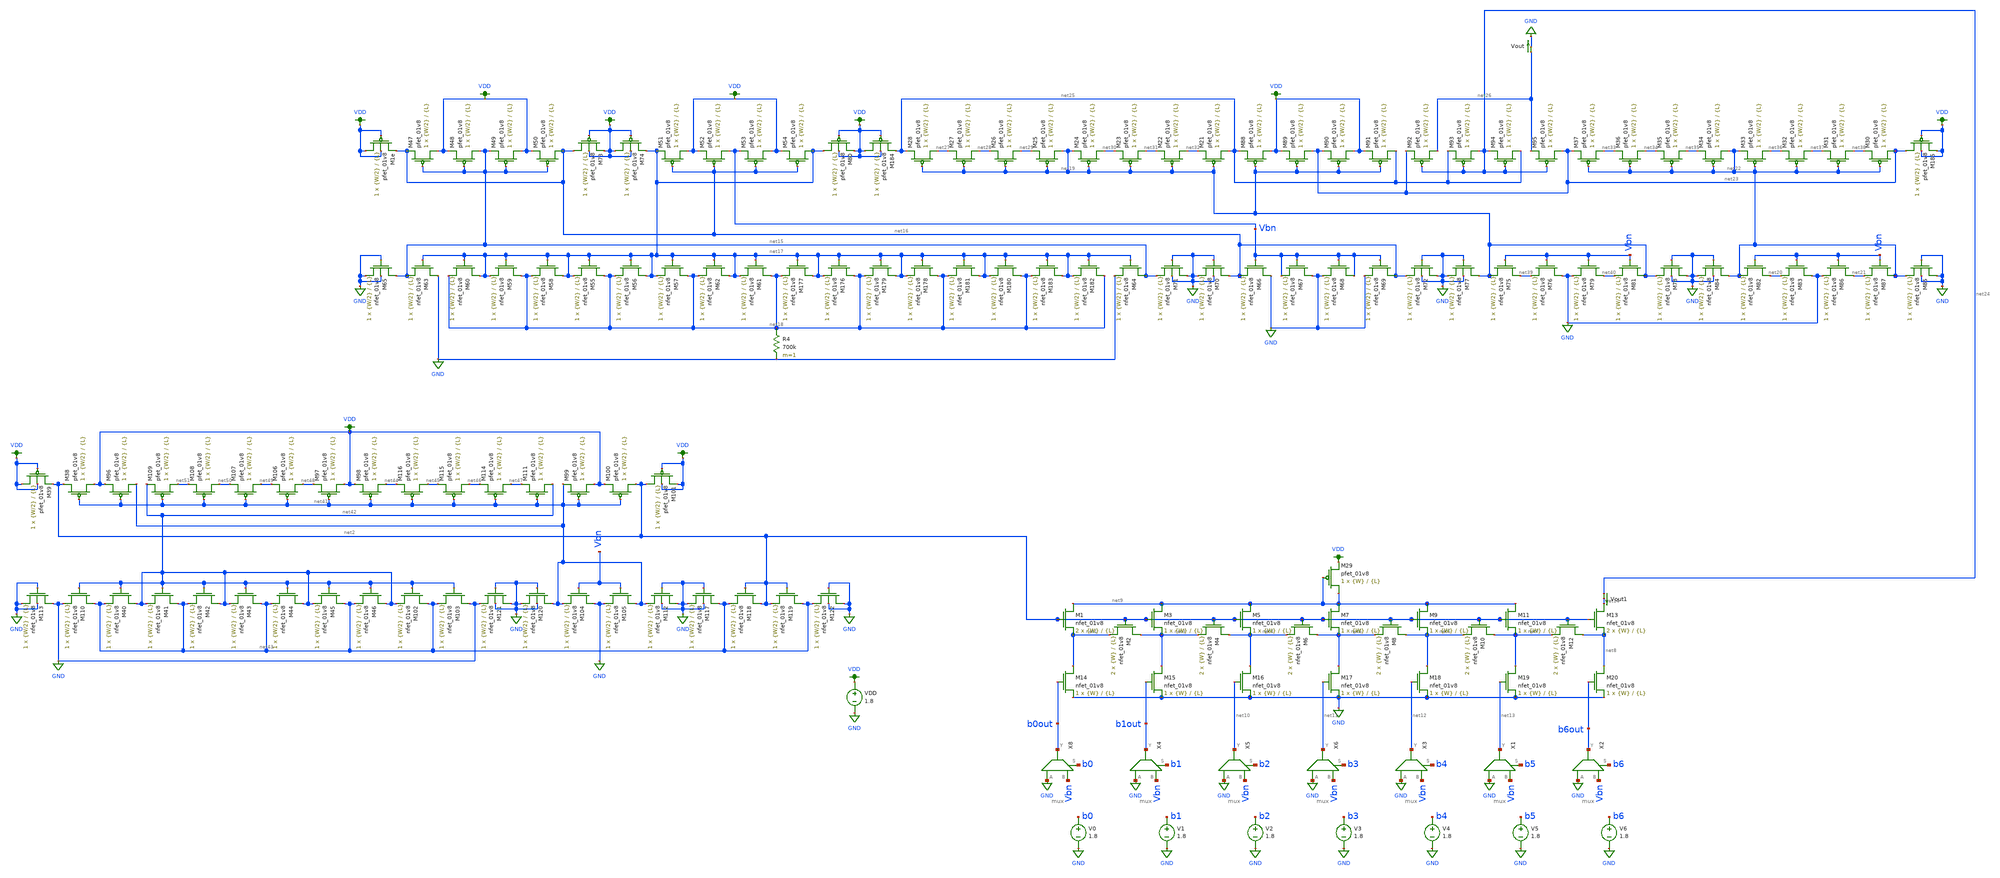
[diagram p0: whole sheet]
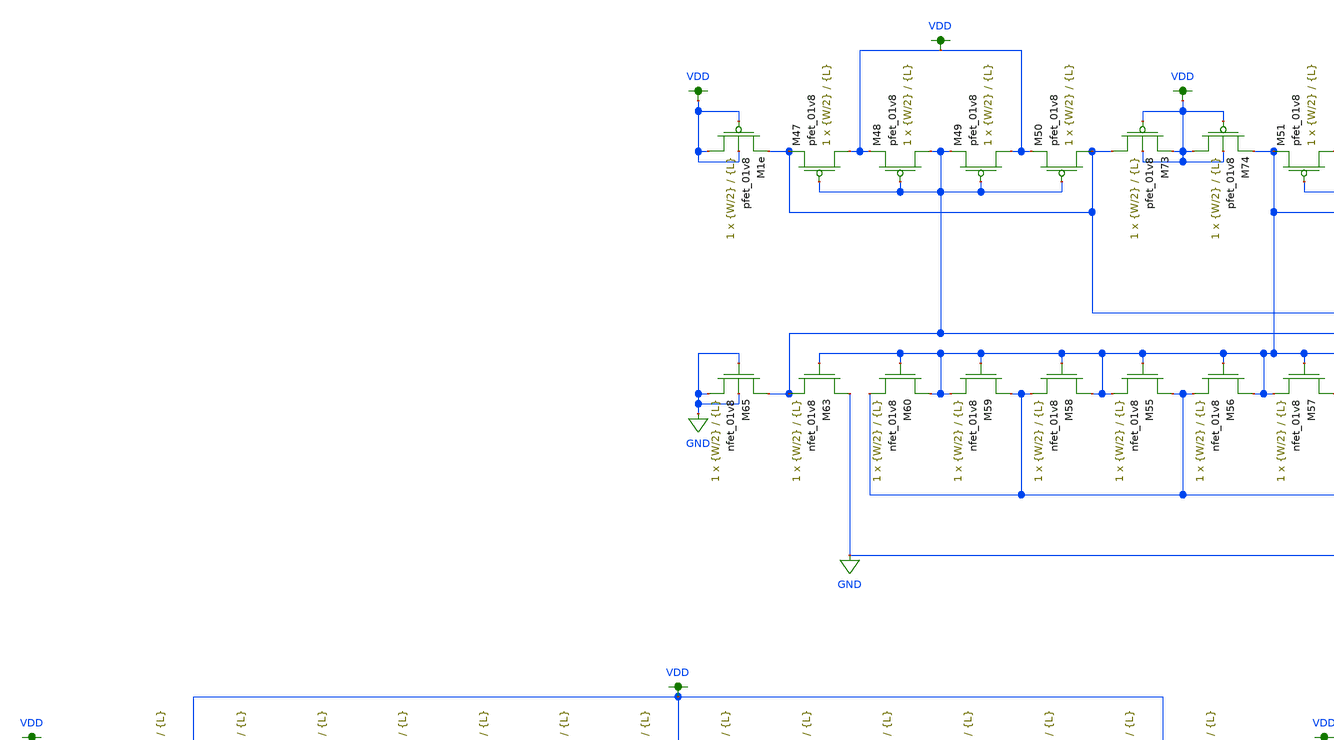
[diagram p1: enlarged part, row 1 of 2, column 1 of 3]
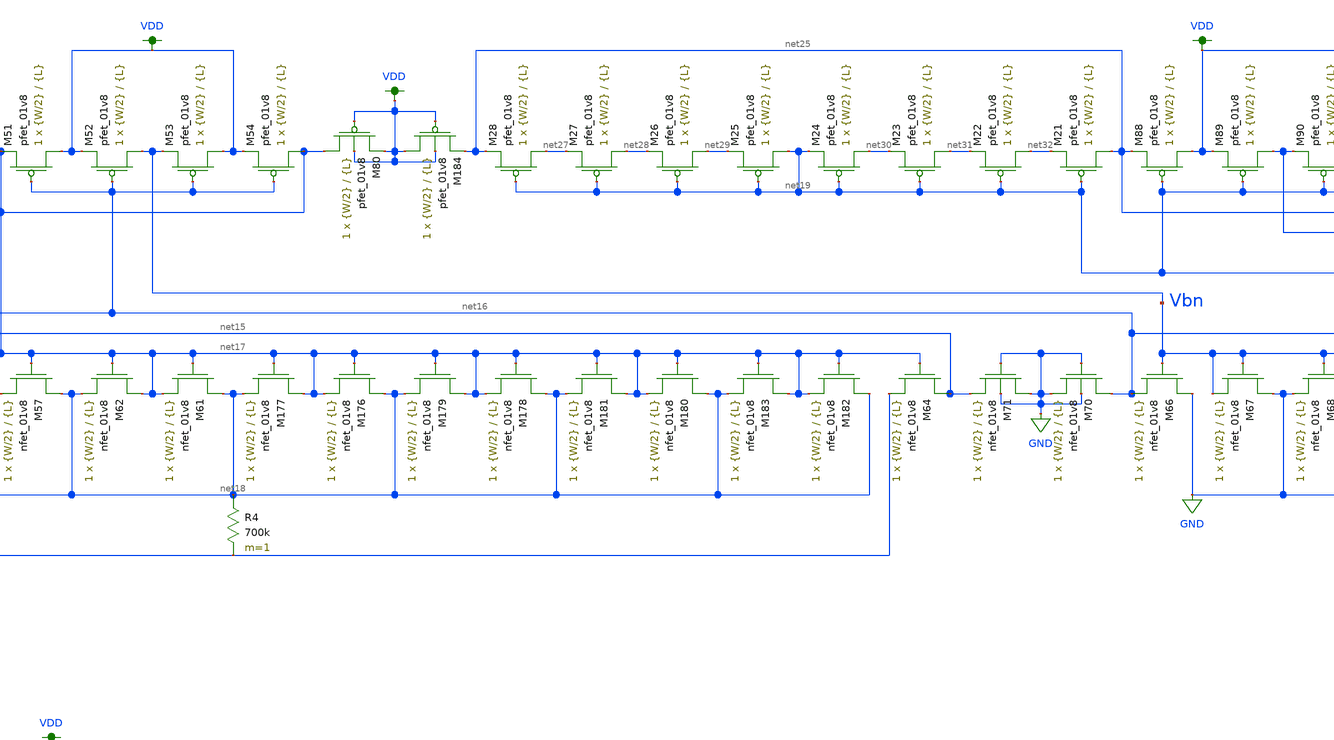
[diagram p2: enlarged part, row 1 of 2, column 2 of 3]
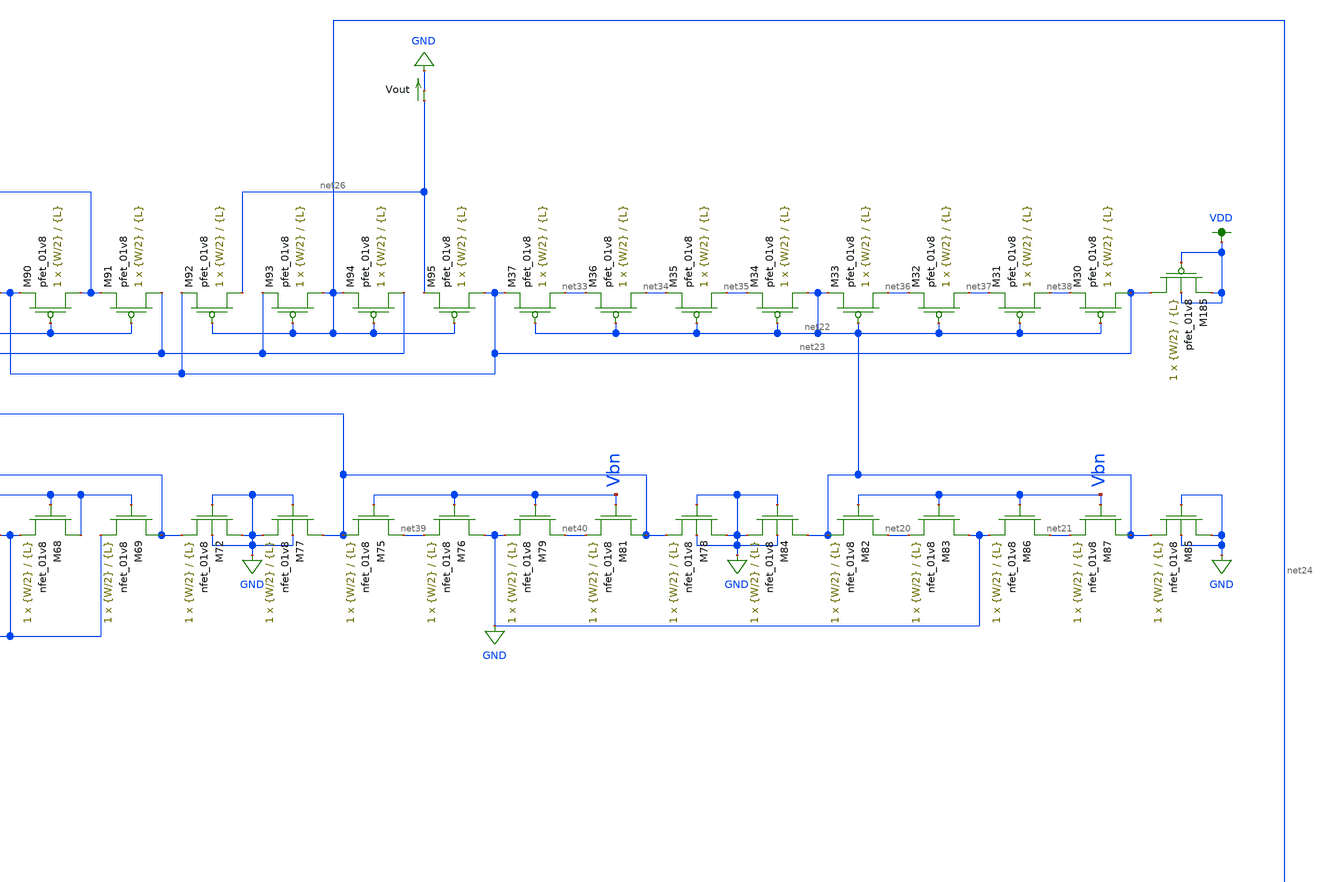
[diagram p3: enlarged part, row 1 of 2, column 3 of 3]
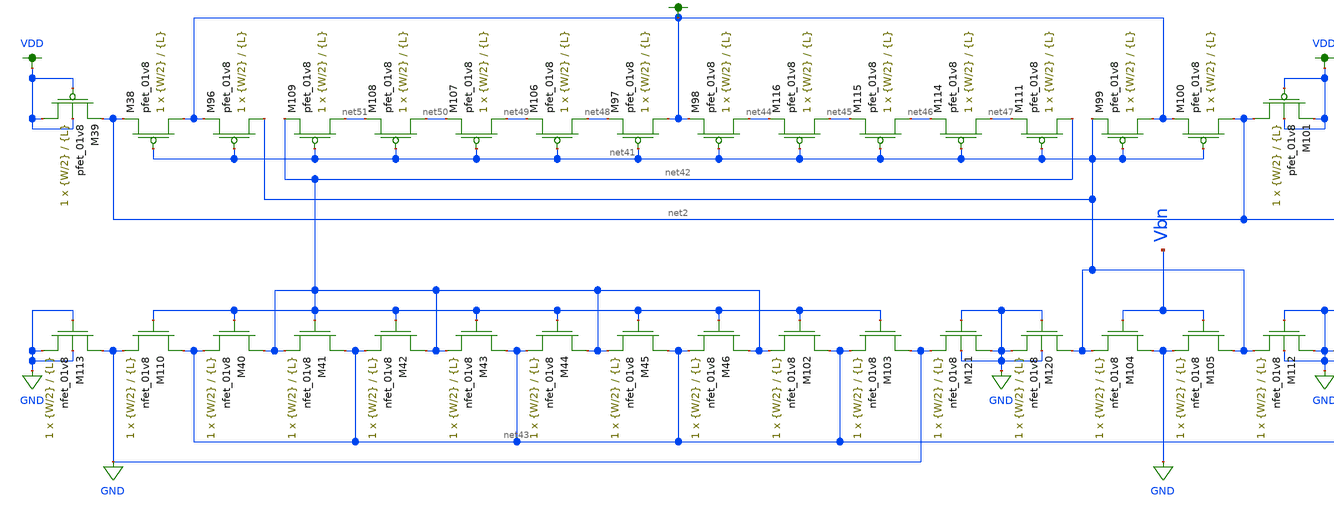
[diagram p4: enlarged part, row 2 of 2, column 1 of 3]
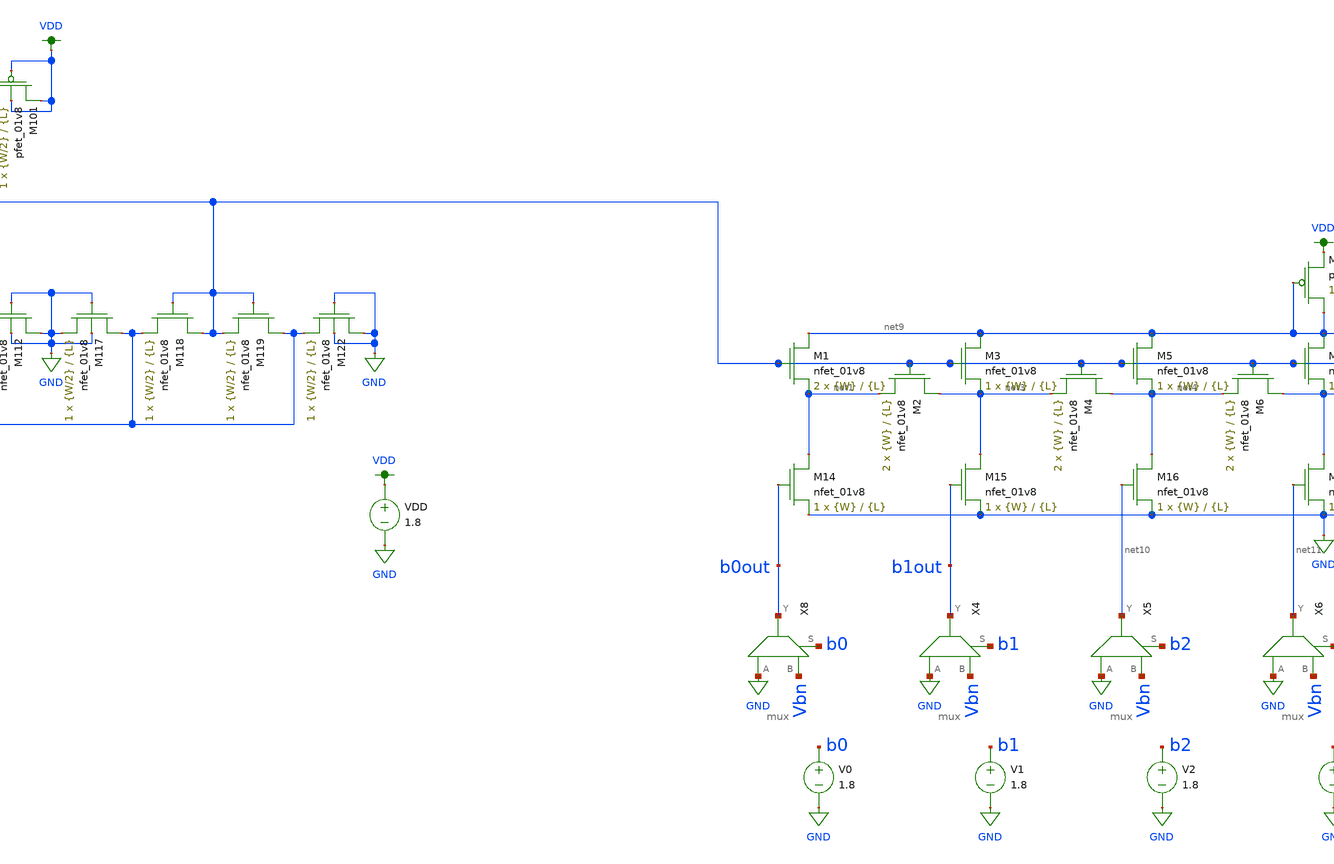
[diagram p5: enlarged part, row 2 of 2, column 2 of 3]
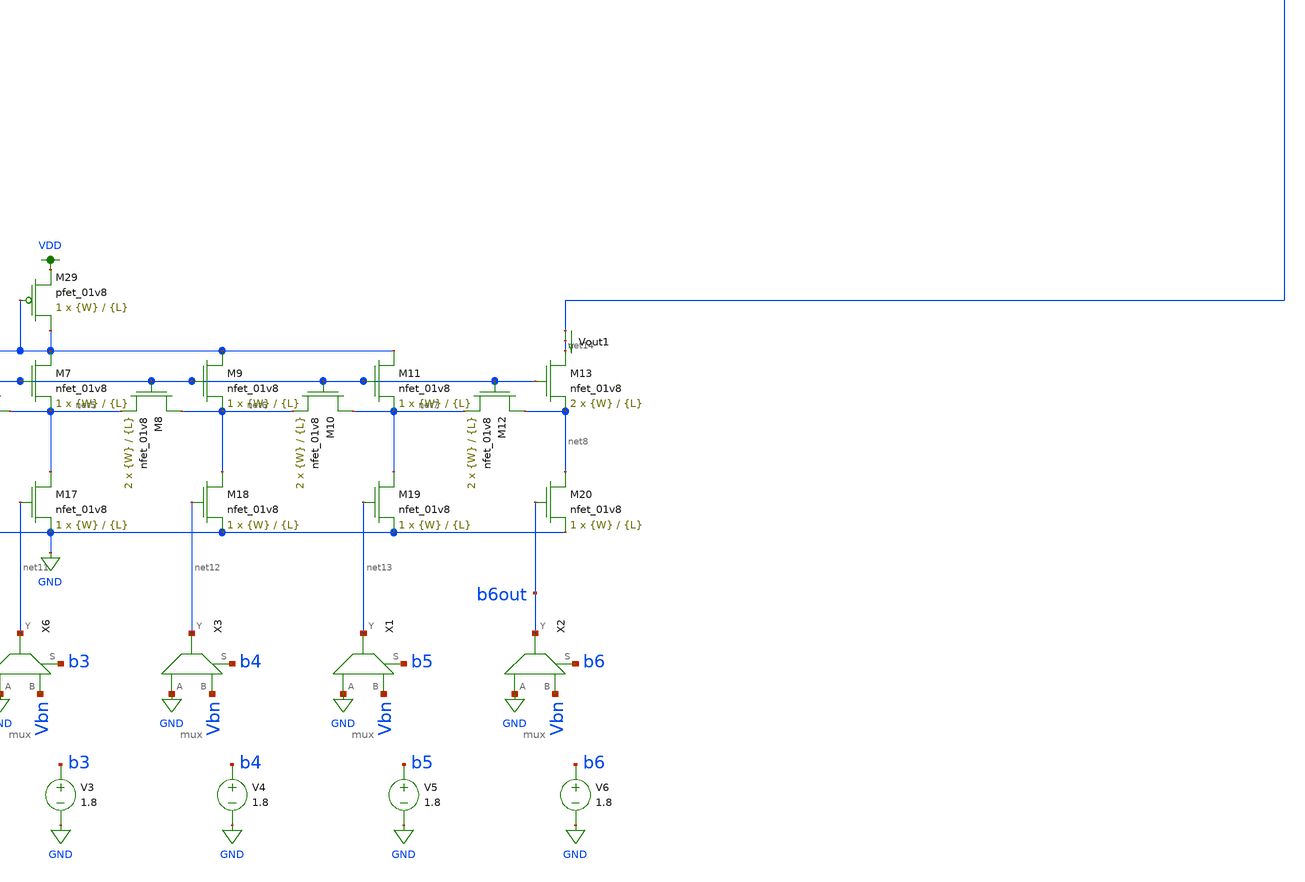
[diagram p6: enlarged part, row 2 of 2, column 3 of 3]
** sch_path: schematics/dac_dnl_inl_current_mirror_lds.sch
**.subckt dac_dnl_inl_current_mirror_lds
XM1 net9 net2 net1 GND sky130_fd_pr__nfet_01v8 L={L} W={W} nf=1 ad='int((nf+1)/2) * W/nf * 0.29' as='int((nf+2)/2) * W/nf * 0.29'
+ pd='2*int((nf+1)/2) * (W/nf + 0.29)' ps='2*int((nf+2)/2) * (W/nf + 0.29)' nrd='0.29 / W' nrs='0.29 / W'
+ sa=0 sb=0 sd=0 mult=2 m=2
XM2 net3 net2 net1 GND sky130_fd_pr__nfet_01v8 L={L} W={W} nf=1 ad='int((nf+1)/2) * W/nf * 0.29' as='int((nf+2)/2) * W/nf * 0.29'
+ pd='2*int((nf+1)/2) * (W/nf + 0.29)' ps='2*int((nf+2)/2) * (W/nf + 0.29)' nrd='0.29 / W' nrs='0.29 / W'
+ sa=0 sb=0 sd=0 mult=2 m=2
XM3 net9 net2 net3 GND sky130_fd_pr__nfet_01v8 L={L} W={W} nf=1 ad='int((nf+1)/2) * W/nf * 0.29' as='int((nf+2)/2) * W/nf * 0.29'
+ pd='2*int((nf+1)/2) * (W/nf + 0.29)' ps='2*int((nf+2)/2) * (W/nf + 0.29)' nrd='0.29 / W' nrs='0.29 / W'
+ sa=0 sb=0 sd=0 mult=1 m=1
XM4 net4 net2 net3 GND sky130_fd_pr__nfet_01v8 L={L} W={W} nf=1 ad='int((nf+1)/2) * W/nf * 0.29' as='int((nf+2)/2) * W/nf * 0.29'
+ pd='2*int((nf+1)/2) * (W/nf + 0.29)' ps='2*int((nf+2)/2) * (W/nf + 0.29)' nrd='0.29 / W' nrs='0.29 / W'
+ sa=0 sb=0 sd=0 mult=2 m=2
XM5 net9 net2 net4 GND sky130_fd_pr__nfet_01v8 L={L} W={W} nf=1 ad='int((nf+1)/2) * W/nf * 0.29' as='int((nf+2)/2) * W/nf * 0.29'
+ pd='2*int((nf+1)/2) * (W/nf + 0.29)' ps='2*int((nf+2)/2) * (W/nf + 0.29)' nrd='0.29 / W' nrs='0.29 / W'
+ sa=0 sb=0 sd=0 mult=1 m=1
XM6 net5 net2 net4 GND sky130_fd_pr__nfet_01v8 L={L} W={W} nf=1 ad='int((nf+1)/2) * W/nf * 0.29' as='int((nf+2)/2) * W/nf * 0.29'
+ pd='2*int((nf+1)/2) * (W/nf + 0.29)' ps='2*int((nf+2)/2) * (W/nf + 0.29)' nrd='0.29 / W' nrs='0.29 / W'
+ sa=0 sb=0 sd=0 mult=2 m=2
XM7 net9 net2 net5 GND sky130_fd_pr__nfet_01v8 L={L} W={W} nf=1 ad='int((nf+1)/2) * W/nf * 0.29' as='int((nf+2)/2) * W/nf * 0.29'
+ pd='2*int((nf+1)/2) * (W/nf + 0.29)' ps='2*int((nf+2)/2) * (W/nf + 0.29)' nrd='0.29 / W' nrs='0.29 / W'
+ sa=0 sb=0 sd=0 mult=1 m=1
XM8 net6 net2 net5 GND sky130_fd_pr__nfet_01v8 L={L} W={W} nf=1 ad='int((nf+1)/2) * W/nf * 0.29' as='int((nf+2)/2) * W/nf * 0.29'
+ pd='2*int((nf+1)/2) * (W/nf + 0.29)' ps='2*int((nf+2)/2) * (W/nf + 0.29)' nrd='0.29 / W' nrs='0.29 / W'
+ sa=0 sb=0 sd=0 mult=2 m=2
XM9 net9 net2 net6 GND sky130_fd_pr__nfet_01v8 L={L} W={W} nf=1 ad='int((nf+1)/2) * W/nf * 0.29' as='int((nf+2)/2) * W/nf * 0.29'
+ pd='2*int((nf+1)/2) * (W/nf + 0.29)' ps='2*int((nf+2)/2) * (W/nf + 0.29)' nrd='0.29 / W' nrs='0.29 / W'
+ sa=0 sb=0 sd=0 mult=1 m=1
XM10 net7 net2 net6 GND sky130_fd_pr__nfet_01v8 L={L} W={W} nf=1 ad='int((nf+1)/2) * W/nf * 0.29' as='int((nf+2)/2) * W/nf * 0.29'
+ pd='2*int((nf+1)/2) * (W/nf + 0.29)' ps='2*int((nf+2)/2) * (W/nf + 0.29)' nrd='0.29 / W' nrs='0.29 / W'
+ sa=0 sb=0 sd=0 mult=2 m=2
XM11 net9 net2 net7 GND sky130_fd_pr__nfet_01v8 L={L} W={W} nf=1 ad='int((nf+1)/2) * W/nf * 0.29' as='int((nf+2)/2) * W/nf * 0.29'
+ pd='2*int((nf+1)/2) * (W/nf + 0.29)' ps='2*int((nf+2)/2) * (W/nf + 0.29)' nrd='0.29 / W' nrs='0.29 / W'
+ sa=0 sb=0 sd=0 mult=1 m=1
XM12 net8 net2 net7 GND sky130_fd_pr__nfet_01v8 L={L} W={W} nf=1 ad='int((nf+1)/2) * W/nf * 0.29' as='int((nf+2)/2) * W/nf * 0.29'
+ pd='2*int((nf+1)/2) * (W/nf + 0.29)' ps='2*int((nf+2)/2) * (W/nf + 0.29)' nrd='0.29 / W' nrs='0.29 / W'
+ sa=0 sb=0 sd=0 mult=2 m=2
XM13 net14 net2 net8 GND sky130_fd_pr__nfet_01v8 L={L} W={W} nf=1 ad='int((nf+1)/2) * W/nf * 0.29' as='int((nf+2)/2) * W/nf * 0.29'
+ pd='2*int((nf+1)/2) * (W/nf + 0.29)' ps='2*int((nf+2)/2) * (W/nf + 0.29)' nrd='0.29 / W' nrs='0.29 / W'
+ sa=0 sb=0 sd=0 mult=2 m=2
XM14 net1 b0out GND GND sky130_fd_pr__nfet_01v8 L={L} W={W} nf=1 ad='int((nf+1)/2) * W/nf * 0.29' as='int((nf+2)/2) * W/nf * 0.29'
+ pd='2*int((nf+1)/2) * (W/nf + 0.29)' ps='2*int((nf+2)/2) * (W/nf + 0.29)' nrd='0.29 / W' nrs='0.29 / W'
+ sa=0 sb=0 sd=0 mult=1 m=1
XM15 net3 b1out GND GND sky130_fd_pr__nfet_01v8 L={L} W={W} nf=1 ad='int((nf+1)/2) * W/nf * 0.29' as='int((nf+2)/2) * W/nf * 0.29'
+ pd='2*int((nf+1)/2) * (W/nf + 0.29)' ps='2*int((nf+2)/2) * (W/nf + 0.29)' nrd='0.29 / W' nrs='0.29 / W'
+ sa=0 sb=0 sd=0 mult=1 m=1
XM16 net4 net10 GND GND sky130_fd_pr__nfet_01v8 L={L} W={W} nf=1 ad='int((nf+1)/2) * W/nf * 0.29' as='int((nf+2)/2) * W/nf * 0.29'
+ pd='2*int((nf+1)/2) * (W/nf + 0.29)' ps='2*int((nf+2)/2) * (W/nf + 0.29)' nrd='0.29 / W' nrs='0.29 / W'
+ sa=0 sb=0 sd=0 mult=1 m=1
XM17 net5 net11 GND GND sky130_fd_pr__nfet_01v8 L={L} W={W} nf=1 ad='int((nf+1)/2) * W/nf * 0.29' as='int((nf+2)/2) * W/nf * 0.29'
+ pd='2*int((nf+1)/2) * (W/nf + 0.29)' ps='2*int((nf+2)/2) * (W/nf + 0.29)' nrd='0.29 / W' nrs='0.29 / W'
+ sa=0 sb=0 sd=0 mult=1 m=1
XM18 net6 net12 GND GND sky130_fd_pr__nfet_01v8 L={L} W={W} nf=1 ad='int((nf+1)/2) * W/nf * 0.29' as='int((nf+2)/2) * W/nf * 0.29'
+ pd='2*int((nf+1)/2) * (W/nf + 0.29)' ps='2*int((nf+2)/2) * (W/nf + 0.29)' nrd='0.29 / W' nrs='0.29 / W'
+ sa=0 sb=0 sd=0 mult=1 m=1
XM19 net7 net13 GND GND sky130_fd_pr__nfet_01v8 L={L} W={W} nf=1 ad='int((nf+1)/2) * W/nf * 0.29' as='int((nf+2)/2) * W/nf * 0.29'
+ pd='2*int((nf+1)/2) * (W/nf + 0.29)' ps='2*int((nf+2)/2) * (W/nf + 0.29)' nrd='0.29 / W' nrs='0.29 / W'
+ sa=0 sb=0 sd=0 mult=1 m=1
XM20 net8 b6out GND GND sky130_fd_pr__nfet_01v8 L={L} W={W} nf=1 ad='int((nf+1)/2) * W/nf * 0.29' as='int((nf+2)/2) * W/nf * 0.29'
+ pd='2*int((nf+1)/2) * (W/nf + 0.29)' ps='2*int((nf+2)/2) * (W/nf + 0.29)' nrd='0.29 / W' nrs='0.29 / W'
+ sa=0 sb=0 sd=0 mult=1 m=1
V0 b0 GND 1.8
V1 b1 GND 1.8
V2 b2 GND 1.8
V3 b3 GND 1.8
V4 b4 GND 1.8
V5 b5 GND 1.8
V6 b6 GND 1.8
VDD VDD GND 1.8
XM29 net9 net9 VDD VDD sky130_fd_pr__pfet_01v8 L={L} W={W} nf=1 ad='int((nf+1)/2) * W/nf * 0.29' as='int((nf+2)/2) * W/nf * 0.29'
+ pd='2*int((nf+1)/2) * (W/nf + 0.29)' ps='2*int((nf+2)/2) * (W/nf + 0.29)' nrd='0.29 / W' nrs='0.29 / W'
+ sa=0 sb=0 sd=0 mult=1 m=1
X8 GND Vbn b0out b0 mux
X4 GND Vbn b1out b1 mux
X5 GND Vbn net10 b2 mux
X6 GND Vbn net11 b3 mux
X3 GND Vbn net12 b4 mux
X1 GND Vbn net13 b5 mux
X2 GND Vbn b6out b6 mux
Vout1 net24 net14 0
.save i(vout1)
XM47 VDD net15 net16 VDD sky130_fd_pr__pfet_01v8 L={L} W={W/2} nf=1 ad='int((nf+1)/2) * W/nf * 0.29'
+ as='int((nf+2)/2) * W/nf * 0.29' pd='2*int((nf+1)/2) * (W/nf + 0.29)' ps='2*int((nf+2)/2) * (W/nf + 0.29)'
+ nrd='0.29 / W' nrs='0.29 / W' sa=0 sb=0 sd=0 mult=1 m=1
XM48 net15 net15 VDD VDD sky130_fd_pr__pfet_01v8 L={L} W={W/2} nf=1 ad='int((nf+1)/2) * W/nf * 0.29'
+ as='int((nf+2)/2) * W/nf * 0.29' pd='2*int((nf+1)/2) * (W/nf + 0.29)' ps='2*int((nf+2)/2) * (W/nf + 0.29)'
+ nrd='0.29 / W' nrs='0.29 / W' sa=0 sb=0 sd=0 mult=1 m=1
XM49 VDD net15 net15 VDD sky130_fd_pr__pfet_01v8 L={L} W={W/2} nf=1 ad='int((nf+1)/2) * W/nf * 0.29'
+ as='int((nf+2)/2) * W/nf * 0.29' pd='2*int((nf+1)/2) * (W/nf + 0.29)' ps='2*int((nf+2)/2) * (W/nf + 0.29)'
+ nrd='0.29 / W' nrs='0.29 / W' sa=0 sb=0 sd=0 mult=1 m=1
XM50 net16 net15 VDD VDD sky130_fd_pr__pfet_01v8 L={L} W={W/2} nf=1 ad='int((nf+1)/2) * W/nf * 0.29'
+ as='int((nf+2)/2) * W/nf * 0.29' pd='2*int((nf+1)/2) * (W/nf + 0.29)' ps='2*int((nf+2)/2) * (W/nf + 0.29)'
+ nrd='0.29 / W' nrs='0.29 / W' sa=0 sb=0 sd=0 mult=1 m=1
XM51 VDD net16 net17 VDD sky130_fd_pr__pfet_01v8 L={L} W={W/2} nf=1 ad='int((nf+1)/2) * W/nf * 0.29'
+ as='int((nf+2)/2) * W/nf * 0.29' pd='2*int((nf+1)/2) * (W/nf + 0.29)' ps='2*int((nf+2)/2) * (W/nf + 0.29)'
+ nrd='0.29 / W' nrs='0.29 / W' sa=0 sb=0 sd=0 mult=1 m=1
XM52 Vbn net16 VDD VDD sky130_fd_pr__pfet_01v8 L={L} W={W/2} nf=1 ad='int((nf+1)/2) * W/nf * 0.29' as='int((nf+2)/2) * W/nf * 0.29'
+ pd='2*int((nf+1)/2) * (W/nf + 0.29)' ps='2*int((nf+2)/2) * (W/nf + 0.29)' nrd='0.29 / W' nrs='0.29 / W'
+ sa=0 sb=0 sd=0 mult=1 m=1
XM53 VDD net16 Vbn VDD sky130_fd_pr__pfet_01v8 L={L} W={W/2} nf=1 ad='int((nf+1)/2) * W/nf * 0.29' as='int((nf+2)/2) * W/nf * 0.29'
+ pd='2*int((nf+1)/2) * (W/nf + 0.29)' ps='2*int((nf+2)/2) * (W/nf + 0.29)' nrd='0.29 / W' nrs='0.29 / W'
+ sa=0 sb=0 sd=0 mult=1 m=1
XM54 net17 net16 VDD VDD sky130_fd_pr__pfet_01v8 L={L} W={W/2} nf=1 ad='int((nf+1)/2) * W/nf * 0.29'
+ as='int((nf+2)/2) * W/nf * 0.29' pd='2*int((nf+1)/2) * (W/nf + 0.29)' ps='2*int((nf+2)/2) * (W/nf + 0.29)'
+ nrd='0.29 / W' nrs='0.29 / W' sa=0 sb=0 sd=0 mult=1 m=1
XM55 net18 net17 net17 GND sky130_fd_pr__nfet_01v8 L={L} W={W/2} nf=1 ad='int((nf+1)/2) * W/nf * 0.29'
+ as='int((nf+2)/2) * W/nf * 0.29' pd='2*int((nf+1)/2) * (W/nf + 0.29)' ps='2*int((nf+2)/2) * (W/nf + 0.29)'
+ nrd='0.29 / W' nrs='0.29 / W' sa=0 sb=0 sd=0 mult=1 m=1
XM56 net17 net17 net18 GND sky130_fd_pr__nfet_01v8 L={L} W={W/2} nf=1 ad='int((nf+1)/2) * W/nf * 0.29'
+ as='int((nf+2)/2) * W/nf * 0.29' pd='2*int((nf+1)/2) * (W/nf + 0.29)' ps='2*int((nf+2)/2) * (W/nf + 0.29)'
+ nrd='0.29 / W' nrs='0.29 / W' sa=0 sb=0 sd=0 mult=1 m=1
XM57 net18 net17 net17 GND sky130_fd_pr__nfet_01v8 L={L} W={W/2} nf=1 ad='int((nf+1)/2) * W/nf * 0.29'
+ as='int((nf+2)/2) * W/nf * 0.29' pd='2*int((nf+1)/2) * (W/nf + 0.29)' ps='2*int((nf+2)/2) * (W/nf + 0.29)'
+ nrd='0.29 / W' nrs='0.29 / W' sa=0 sb=0 sd=0 mult=1 m=1
XM58 net17 net17 net18 GND sky130_fd_pr__nfet_01v8 L={L} W={W/2} nf=1 ad='int((nf+1)/2) * W/nf * 0.29'
+ as='int((nf+2)/2) * W/nf * 0.29' pd='2*int((nf+1)/2) * (W/nf + 0.29)' ps='2*int((nf+2)/2) * (W/nf + 0.29)'
+ nrd='0.29 / W' nrs='0.29 / W' sa=0 sb=0 sd=0 mult=1 m=1
XM59 net18 net17 net17 GND sky130_fd_pr__nfet_01v8 L={L} W={W/2} nf=1 ad='int((nf+1)/2) * W/nf * 0.29'
+ as='int((nf+2)/2) * W/nf * 0.29' pd='2*int((nf+1)/2) * (W/nf + 0.29)' ps='2*int((nf+2)/2) * (W/nf + 0.29)'
+ nrd='0.29 / W' nrs='0.29 / W' sa=0 sb=0 sd=0 mult=1 m=1
XM60 net17 net17 net18 GND sky130_fd_pr__nfet_01v8 L={L} W={W/2} nf=1 ad='int((nf+1)/2) * W/nf * 0.29'
+ as='int((nf+2)/2) * W/nf * 0.29' pd='2*int((nf+1)/2) * (W/nf + 0.29)' ps='2*int((nf+2)/2) * (W/nf + 0.29)'
+ nrd='0.29 / W' nrs='0.29 / W' sa=0 sb=0 sd=0 mult=1 m=1
XM61 net18 net17 net17 GND sky130_fd_pr__nfet_01v8 L={L} W={W/2} nf=1 ad='int((nf+1)/2) * W/nf * 0.29'
+ as='int((nf+2)/2) * W/nf * 0.29' pd='2*int((nf+1)/2) * (W/nf + 0.29)' ps='2*int((nf+2)/2) * (W/nf + 0.29)'
+ nrd='0.29 / W' nrs='0.29 / W' sa=0 sb=0 sd=0 mult=1 m=1
XM62 net17 net17 net18 GND sky130_fd_pr__nfet_01v8 L={L} W={W/2} nf=1 ad='int((nf+1)/2) * W/nf * 0.29'
+ as='int((nf+2)/2) * W/nf * 0.29' pd='2*int((nf+1)/2) * (W/nf + 0.29)' ps='2*int((nf+2)/2) * (W/nf + 0.29)'
+ nrd='0.29 / W' nrs='0.29 / W' sa=0 sb=0 sd=0 mult=1 m=1
XM63 GND net17 net15 GND sky130_fd_pr__nfet_01v8 L={L} W={W/2} nf=1 ad='int((nf+1)/2) * W/nf * 0.29'
+ as='int((nf+2)/2) * W/nf * 0.29' pd='2*int((nf+1)/2) * (W/nf + 0.29)' ps='2*int((nf+2)/2) * (W/nf + 0.29)'
+ nrd='0.29 / W' nrs='0.29 / W' sa=0 sb=0 sd=0 mult=1 m=1
XM64 net15 net17 GND GND sky130_fd_pr__nfet_01v8 L={L} W={W/2} nf=1 ad='int((nf+1)/2) * W/nf * 0.29'
+ as='int((nf+2)/2) * W/nf * 0.29' pd='2*int((nf+1)/2) * (W/nf + 0.29)' ps='2*int((nf+2)/2) * (W/nf + 0.29)'
+ nrd='0.29 / W' nrs='0.29 / W' sa=0 sb=0 sd=0 mult=1 m=1
R4 net18 GND 700k m=1
XM1e VDD VDD net16 VDD sky130_fd_pr__pfet_01v8 L={L} W={W/2} nf=1 ad='int((nf+1)/2) * W/nf * 0.29' as='int((nf+2)/2) * W/nf * 0.29'
+ pd='2*int((nf+1)/2) * (W/nf + 0.29)' ps='2*int((nf+2)/2) * (W/nf + 0.29)' nrd='0.29 / W' nrs='0.29 / W'
+ sa=0 sb=0 sd=0 mult=1 m=1
XM65 net15 GND GND GND sky130_fd_pr__nfet_01v8 L={L} W={W/2} nf=1 ad='int((nf+1)/2) * W/nf * 0.29' as='int((nf+2)/2) * W/nf * 0.29'
+ pd='2*int((nf+1)/2) * (W/nf + 0.29)' ps='2*int((nf+2)/2) * (W/nf + 0.29)' nrd='0.29 / W' nrs='0.29 / W'
+ sa=0 sb=0 sd=0 mult=1 m=1
XM66 GND Vbn net16 GND sky130_fd_pr__nfet_01v8 L={L} W={W/2} nf=1 ad='int((nf+1)/2) * W/nf * 0.29' as='int((nf+2)/2) * W/nf * 0.29'
+ pd='2*int((nf+1)/2) * (W/nf + 0.29)' ps='2*int((nf+2)/2) * (W/nf + 0.29)' nrd='0.29 / W' nrs='0.29 / W'
+ sa=0 sb=0 sd=0 mult=1 m=1
XM67 GND Vbn Vbn GND sky130_fd_pr__nfet_01v8 L={L} W={W/2} nf=1 ad='int((nf+1)/2) * W/nf * 0.29' as='int((nf+2)/2) * W/nf * 0.29'
+ pd='2*int((nf+1)/2) * (W/nf + 0.29)' ps='2*int((nf+2)/2) * (W/nf + 0.29)' nrd='0.29 / W' nrs='0.29 / W'
+ sa=0 sb=0 sd=0 mult=1 m=1
XM68 Vbn Vbn GND GND sky130_fd_pr__nfet_01v8 L={L} W={W/2} nf=1 ad='int((nf+1)/2) * W/nf * 0.29' as='int((nf+2)/2) * W/nf * 0.29'
+ pd='2*int((nf+1)/2) * (W/nf + 0.29)' ps='2*int((nf+2)/2) * (W/nf + 0.29)' nrd='0.29 / W' nrs='0.29 / W'
+ sa=0 sb=0 sd=0 mult=1 m=1
XM69 net16 Vbn GND GND sky130_fd_pr__nfet_01v8 L={L} W={W/2} nf=1 ad='int((nf+1)/2) * W/nf * 0.29' as='int((nf+2)/2) * W/nf * 0.29'
+ pd='2*int((nf+1)/2) * (W/nf + 0.29)' ps='2*int((nf+2)/2) * (W/nf + 0.29)' nrd='0.29 / W' nrs='0.29 / W'
+ sa=0 sb=0 sd=0 mult=1 m=1
XM70 net16 GND GND GND sky130_fd_pr__nfet_01v8 L={L} W={W/2} nf=1 ad='int((nf+1)/2) * W/nf * 0.29' as='int((nf+2)/2) * W/nf * 0.29'
+ pd='2*int((nf+1)/2) * (W/nf + 0.29)' ps='2*int((nf+2)/2) * (W/nf + 0.29)' nrd='0.29 / W' nrs='0.29 / W'
+ sa=0 sb=0 sd=0 mult=1 m=1
XM71 GND GND net15 GND sky130_fd_pr__nfet_01v8 L={L} W={W/2} nf=1 ad='int((nf+1)/2) * W/nf * 0.29' as='int((nf+2)/2) * W/nf * 0.29'
+ pd='2*int((nf+1)/2) * (W/nf + 0.29)' ps='2*int((nf+2)/2) * (W/nf + 0.29)' nrd='0.29 / W' nrs='0.29 / W'
+ sa=0 sb=0 sd=0 mult=1 m=1
XM72 GND GND net16 GND sky130_fd_pr__nfet_01v8 L={L} W={W/2} nf=1 ad='int((nf+1)/2) * W/nf * 0.29' as='int((nf+2)/2) * W/nf * 0.29'
+ pd='2*int((nf+1)/2) * (W/nf + 0.29)' ps='2*int((nf+2)/2) * (W/nf + 0.29)' nrd='0.29 / W' nrs='0.29 / W'
+ sa=0 sb=0 sd=0 mult=1 m=1
XM77 net19 GND GND GND sky130_fd_pr__nfet_01v8 L={L} W={W/2} nf=1 ad='int((nf+1)/2) * W/nf * 0.29' as='int((nf+2)/2) * W/nf * 0.29'
+ pd='2*int((nf+1)/2) * (W/nf + 0.29)' ps='2*int((nf+2)/2) * (W/nf + 0.29)' nrd='0.29 / W' nrs='0.29 / W'
+ sa=0 sb=0 sd=0 mult=1 m=1
XM78 GND GND net19 GND sky130_fd_pr__nfet_01v8 L={L} W={W/2} nf=1 ad='int((nf+1)/2) * W/nf * 0.29' as='int((nf+2)/2) * W/nf * 0.29'
+ pd='2*int((nf+1)/2) * (W/nf + 0.29)' ps='2*int((nf+2)/2) * (W/nf + 0.29)' nrd='0.29 / W' nrs='0.29 / W'
+ sa=0 sb=0 sd=0 mult=1 m=1
XM73 net16 VDD VDD VDD sky130_fd_pr__pfet_01v8 L={L} W={W/2} nf=1 ad='int((nf+1)/2) * W/nf * 0.29' as='int((nf+2)/2) * W/nf * 0.29'
+ pd='2*int((nf+1)/2) * (W/nf + 0.29)' ps='2*int((nf+2)/2) * (W/nf + 0.29)' nrd='0.29 / W' nrs='0.29 / W'
+ sa=0 sb=0 sd=0 mult=1 m=1
XM74 VDD VDD net17 VDD sky130_fd_pr__pfet_01v8 L={L} W={W/2} nf=1 ad='int((nf+1)/2) * W/nf * 0.29' as='int((nf+2)/2) * W/nf * 0.29'
+ pd='2*int((nf+1)/2) * (W/nf + 0.29)' ps='2*int((nf+2)/2) * (W/nf + 0.29)' nrd='0.29 / W' nrs='0.29 / W'
+ sa=0 sb=0 sd=0 mult=1 m=1
XM80 net17 VDD VDD VDD sky130_fd_pr__pfet_01v8 L={L} W={W/2} nf=1 ad='int((nf+1)/2) * W/nf * 0.29' as='int((nf+2)/2) * W/nf * 0.29'
+ pd='2*int((nf+1)/2) * (W/nf + 0.29)' ps='2*int((nf+2)/2) * (W/nf + 0.29)' nrd='0.29 / W' nrs='0.29 / W'
+ sa=0 sb=0 sd=0 mult=1 m=1
XM84 net22 GND GND GND sky130_fd_pr__nfet_01v8 L={L} W={W/2} nf=1 ad='int((nf+1)/2) * W/nf * 0.29' as='int((nf+2)/2) * W/nf * 0.29'
+ pd='2*int((nf+1)/2) * (W/nf + 0.29)' ps='2*int((nf+2)/2) * (W/nf + 0.29)' nrd='0.29 / W' nrs='0.29 / W'
+ sa=0 sb=0 sd=0 mult=1 m=1
XM85 GND GND net22 GND sky130_fd_pr__nfet_01v8 L={L} W={W/2} nf=1 ad='int((nf+1)/2) * W/nf * 0.29' as='int((nf+2)/2) * W/nf * 0.29'
+ pd='2*int((nf+1)/2) * (W/nf + 0.29)' ps='2*int((nf+2)/2) * (W/nf + 0.29)' nrd='0.29 / W' nrs='0.29 / W'
+ sa=0 sb=0 sd=0 mult=1 m=1
XM75 net39 Vbn net19 GND sky130_fd_pr__nfet_01v8 L={L} W={W/2} nf=1 ad='int((nf+1)/2) * W/nf * 0.29'
+ as='int((nf+2)/2) * W/nf * 0.29' pd='2*int((nf+1)/2) * (W/nf + 0.29)' ps='2*int((nf+2)/2) * (W/nf + 0.29)'
+ nrd='0.29 / W' nrs='0.29 / W' sa=0 sb=0 sd=0 mult=1 m=1
XM76 GND Vbn net39 GND sky130_fd_pr__nfet_01v8 L={L} W={W/2} nf=1 ad='int((nf+1)/2) * W/nf * 0.29' as='int((nf+2)/2) * W/nf * 0.29'
+ pd='2*int((nf+1)/2) * (W/nf + 0.29)' ps='2*int((nf+2)/2) * (W/nf + 0.29)' nrd='0.29 / W' nrs='0.29 / W'
+ sa=0 sb=0 sd=0 mult=1 m=1
XM79 net40 Vbn GND GND sky130_fd_pr__nfet_01v8 L={L} W={W/2} nf=1 ad='int((nf+1)/2) * W/nf * 0.29' as='int((nf+2)/2) * W/nf * 0.29'
+ pd='2*int((nf+1)/2) * (W/nf + 0.29)' ps='2*int((nf+2)/2) * (W/nf + 0.29)' nrd='0.29 / W' nrs='0.29 / W'
+ sa=0 sb=0 sd=0 mult=1 m=1
XM81 net19 Vbn net40 GND sky130_fd_pr__nfet_01v8 L={L} W={W/2} nf=1 ad='int((nf+1)/2) * W/nf * 0.29'
+ as='int((nf+2)/2) * W/nf * 0.29' pd='2*int((nf+1)/2) * (W/nf + 0.29)' ps='2*int((nf+2)/2) * (W/nf + 0.29)'
+ nrd='0.29 / W' nrs='0.29 / W' sa=0 sb=0 sd=0 mult=1 m=1
XM82 net20 Vbn net22 GND sky130_fd_pr__nfet_01v8 L={L} W={W/2} nf=1 ad='int((nf+1)/2) * W/nf * 0.29'
+ as='int((nf+2)/2) * W/nf * 0.29' pd='2*int((nf+1)/2) * (W/nf + 0.29)' ps='2*int((nf+2)/2) * (W/nf + 0.29)'
+ nrd='0.29 / W' nrs='0.29 / W' sa=0 sb=0 sd=0 mult=1 m=1
XM83 GND Vbn net20 GND sky130_fd_pr__nfet_01v8 L={L} W={W/2} nf=1 ad='int((nf+1)/2) * W/nf * 0.29' as='int((nf+2)/2) * W/nf * 0.29'
+ pd='2*int((nf+1)/2) * (W/nf + 0.29)' ps='2*int((nf+2)/2) * (W/nf + 0.29)' nrd='0.29 / W' nrs='0.29 / W'
+ sa=0 sb=0 sd=0 mult=1 m=1
XM86 net21 Vbn GND GND sky130_fd_pr__nfet_01v8 L={L} W={W/2} nf=1 ad='int((nf+1)/2) * W/nf * 0.29' as='int((nf+2)/2) * W/nf * 0.29'
+ pd='2*int((nf+1)/2) * (W/nf + 0.29)' ps='2*int((nf+2)/2) * (W/nf + 0.29)' nrd='0.29 / W' nrs='0.29 / W'
+ sa=0 sb=0 sd=0 mult=1 m=1
XM87 net22 Vbn net21 GND sky130_fd_pr__nfet_01v8 L={L} W={W/2} nf=1 ad='int((nf+1)/2) * W/nf * 0.29'
+ as='int((nf+2)/2) * W/nf * 0.29' pd='2*int((nf+1)/2) * (W/nf + 0.29)' ps='2*int((nf+2)/2) * (W/nf + 0.29)'
+ nrd='0.29 / W' nrs='0.29 / W' sa=0 sb=0 sd=0 mult=1 m=1
XM88 VDD net19 net25 VDD sky130_fd_pr__pfet_01v8 L={L} W={W/2} nf=1 ad='int((nf+1)/2) * W/nf * 0.29'
+ as='int((nf+2)/2) * W/nf * 0.29' pd='2*int((nf+1)/2) * (W/nf + 0.29)' ps='2*int((nf+2)/2) * (W/nf + 0.29)'
+ nrd='0.29 / W' nrs='0.29 / W' sa=0 sb=0 sd=0 mult=1 m=1
XM89 net23 net19 VDD VDD sky130_fd_pr__pfet_01v8 L={L} W={W/2} nf=1 ad='int((nf+1)/2) * W/nf * 0.29'
+ as='int((nf+2)/2) * W/nf * 0.29' pd='2*int((nf+1)/2) * (W/nf + 0.29)' ps='2*int((nf+2)/2) * (W/nf + 0.29)'
+ nrd='0.29 / W' nrs='0.29 / W' sa=0 sb=0 sd=0 mult=1 m=1
XM90 VDD net19 net23 VDD sky130_fd_pr__pfet_01v8 L={L} W={W/2} nf=1 ad='int((nf+1)/2) * W/nf * 0.29'
+ as='int((nf+2)/2) * W/nf * 0.29' pd='2*int((nf+1)/2) * (W/nf + 0.29)' ps='2*int((nf+2)/2) * (W/nf + 0.29)'
+ nrd='0.29 / W' nrs='0.29 / W' sa=0 sb=0 sd=0 mult=1 m=1
XM91 net25 net19 VDD VDD sky130_fd_pr__pfet_01v8 L={L} W={W/2} nf=1 ad='int((nf+1)/2) * W/nf * 0.29'
+ as='int((nf+2)/2) * W/nf * 0.29' pd='2*int((nf+1)/2) * (W/nf + 0.29)' ps='2*int((nf+2)/2) * (W/nf + 0.29)'
+ nrd='0.29 / W' nrs='0.29 / W' sa=0 sb=0 sd=0 mult=1 m=1
XM92 net26 net24 net23 VDD sky130_fd_pr__pfet_01v8 L={L} W={W/2} nf=1 ad='int((nf+1)/2) * W/nf * 0.29'
+ as='int((nf+2)/2) * W/nf * 0.29' pd='2*int((nf+1)/2) * (W/nf + 0.29)' ps='2*int((nf+2)/2) * (W/nf + 0.29)'
+ nrd='0.29 / W' nrs='0.29 / W' sa=0 sb=0 sd=0 mult=1 m=1
XM93 net24 net24 net25 VDD sky130_fd_pr__pfet_01v8 L={L} W={W/2} nf=1 ad='int((nf+1)/2) * W/nf * 0.29'
+ as='int((nf+2)/2) * W/nf * 0.29' pd='2*int((nf+1)/2) * (W/nf + 0.29)' ps='2*int((nf+2)/2) * (W/nf + 0.29)'
+ nrd='0.29 / W' nrs='0.29 / W' sa=0 sb=0 sd=0 mult=1 m=1
XM94 net25 net24 net24 VDD sky130_fd_pr__pfet_01v8 L={L} W={W/2} nf=1 ad='int((nf+1)/2) * W/nf * 0.29'
+ as='int((nf+2)/2) * W/nf * 0.29' pd='2*int((nf+1)/2) * (W/nf + 0.29)' ps='2*int((nf+2)/2) * (W/nf + 0.29)'
+ nrd='0.29 / W' nrs='0.29 / W' sa=0 sb=0 sd=0 mult=1 m=1
XM95 net23 net24 net26 VDD sky130_fd_pr__pfet_01v8 L={L} W={W/2} nf=1 ad='int((nf+1)/2) * W/nf * 0.29'
+ as='int((nf+2)/2) * W/nf * 0.29' pd='2*int((nf+1)/2) * (W/nf + 0.29)' ps='2*int((nf+2)/2) * (W/nf + 0.29)'
+ nrd='0.29 / W' nrs='0.29 / W' sa=0 sb=0 sd=0 mult=1 m=1
XM176 net18 net17 net17 GND sky130_fd_pr__nfet_01v8 L={L} W={W/2} nf=1 ad='int((nf+1)/2) * W/nf * 0.29'
+ as='int((nf+2)/2) * W/nf * 0.29' pd='2*int((nf+1)/2) * (W/nf + 0.29)' ps='2*int((nf+2)/2) * (W/nf + 0.29)'
+ nrd='0.29 / W' nrs='0.29 / W' sa=0 sb=0 sd=0 mult=1 m=1
XM177 net17 net17 net18 GND sky130_fd_pr__nfet_01v8 L={L} W={W/2} nf=1 ad='int((nf+1)/2) * W/nf * 0.29'
+ as='int((nf+2)/2) * W/nf * 0.29' pd='2*int((nf+1)/2) * (W/nf + 0.29)' ps='2*int((nf+2)/2) * (W/nf + 0.29)'
+ nrd='0.29 / W' nrs='0.29 / W' sa=0 sb=0 sd=0 mult=1 m=1
XM178 net18 net17 net17 GND sky130_fd_pr__nfet_01v8 L={L} W={W/2} nf=1 ad='int((nf+1)/2) * W/nf * 0.29'
+ as='int((nf+2)/2) * W/nf * 0.29' pd='2*int((nf+1)/2) * (W/nf + 0.29)' ps='2*int((nf+2)/2) * (W/nf + 0.29)'
+ nrd='0.29 / W' nrs='0.29 / W' sa=0 sb=0 sd=0 mult=1 m=1
XM179 net17 net17 net18 GND sky130_fd_pr__nfet_01v8 L={L} W={W/2} nf=1 ad='int((nf+1)/2) * W/nf * 0.29'
+ as='int((nf+2)/2) * W/nf * 0.29' pd='2*int((nf+1)/2) * (W/nf + 0.29)' ps='2*int((nf+2)/2) * (W/nf + 0.29)'
+ nrd='0.29 / W' nrs='0.29 / W' sa=0 sb=0 sd=0 mult=1 m=1
XM180 net18 net17 net17 GND sky130_fd_pr__nfet_01v8 L={L} W={W/2} nf=1 ad='int((nf+1)/2) * W/nf * 0.29'
+ as='int((nf+2)/2) * W/nf * 0.29' pd='2*int((nf+1)/2) * (W/nf + 0.29)' ps='2*int((nf+2)/2) * (W/nf + 0.29)'
+ nrd='0.29 / W' nrs='0.29 / W' sa=0 sb=0 sd=0 mult=1 m=1
XM181 net17 net17 net18 GND sky130_fd_pr__nfet_01v8 L={L} W={W/2} nf=1 ad='int((nf+1)/2) * W/nf * 0.29'
+ as='int((nf+2)/2) * W/nf * 0.29' pd='2*int((nf+1)/2) * (W/nf + 0.29)' ps='2*int((nf+2)/2) * (W/nf + 0.29)'
+ nrd='0.29 / W' nrs='0.29 / W' sa=0 sb=0 sd=0 mult=1 m=1
XM182 net18 net17 net17 GND sky130_fd_pr__nfet_01v8 L={L} W={W/2} nf=1 ad='int((nf+1)/2) * W/nf * 0.29'
+ as='int((nf+2)/2) * W/nf * 0.29' pd='2*int((nf+1)/2) * (W/nf + 0.29)' ps='2*int((nf+2)/2) * (W/nf + 0.29)'
+ nrd='0.29 / W' nrs='0.29 / W' sa=0 sb=0 sd=0 mult=1 m=1
XM183 net17 net17 net18 GND sky130_fd_pr__nfet_01v8 L={L} W={W/2} nf=1 ad='int((nf+1)/2) * W/nf * 0.29'
+ as='int((nf+2)/2) * W/nf * 0.29' pd='2*int((nf+1)/2) * (W/nf + 0.29)' ps='2*int((nf+2)/2) * (W/nf + 0.29)'
+ nrd='0.29 / W' nrs='0.29 / W' sa=0 sb=0 sd=0 mult=1 m=1
XM184 VDD VDD net25 VDD sky130_fd_pr__pfet_01v8 L={L} W={W/2} nf=1 ad='int((nf+1)/2) * W/nf * 0.29' as='int((nf+2)/2) * W/nf * 0.29'
+ pd='2*int((nf+1)/2) * (W/nf + 0.29)' ps='2*int((nf+2)/2) * (W/nf + 0.29)' nrd='0.29 / W' nrs='0.29 / W'
+ sa=0 sb=0 sd=0 mult=1 m=1
XM185 net23 VDD VDD VDD sky130_fd_pr__pfet_01v8 L={L} W={W/2} nf=1 ad='int((nf+1)/2) * W/nf * 0.29' as='int((nf+2)/2) * W/nf * 0.29'
+ pd='2*int((nf+1)/2) * (W/nf + 0.29)' ps='2*int((nf+2)/2) * (W/nf + 0.29)' nrd='0.29 / W' nrs='0.29 / W'
+ sa=0 sb=0 sd=0 mult=1 m=1
Vout net26 GND 0
.save i(vout)
XM21 net25 net19 net32 VDD sky130_fd_pr__pfet_01v8 L={L} W={W/2} nf=1 ad='int((nf+1)/2) * W/nf * 0.29'
+ as='int((nf+2)/2) * W/nf * 0.29' pd='2*int((nf+1)/2) * (W/nf + 0.29)' ps='2*int((nf+2)/2) * (W/nf + 0.29)'
+ nrd='0.29 / W' nrs='0.29 / W' sa=0 sb=0 sd=0 mult=1 m=1
XM22 net32 net19 net31 VDD sky130_fd_pr__pfet_01v8 L={L} W={W/2} nf=1 ad='int((nf+1)/2) * W/nf * 0.29'
+ as='int((nf+2)/2) * W/nf * 0.29' pd='2*int((nf+1)/2) * (W/nf + 0.29)' ps='2*int((nf+2)/2) * (W/nf + 0.29)'
+ nrd='0.29 / W' nrs='0.29 / W' sa=0 sb=0 sd=0 mult=1 m=1
XM23 net31 net19 net30 VDD sky130_fd_pr__pfet_01v8 L={L} W={W/2} nf=1 ad='int((nf+1)/2) * W/nf * 0.29'
+ as='int((nf+2)/2) * W/nf * 0.29' pd='2*int((nf+1)/2) * (W/nf + 0.29)' ps='2*int((nf+2)/2) * (W/nf + 0.29)'
+ nrd='0.29 / W' nrs='0.29 / W' sa=0 sb=0 sd=0 mult=1 m=1
XM24 net30 net19 net19 VDD sky130_fd_pr__pfet_01v8 L={L} W={W/2} nf=1 ad='int((nf+1)/2) * W/nf * 0.29'
+ as='int((nf+2)/2) * W/nf * 0.29' pd='2*int((nf+1)/2) * (W/nf + 0.29)' ps='2*int((nf+2)/2) * (W/nf + 0.29)'
+ nrd='0.29 / W' nrs='0.29 / W' sa=0 sb=0 sd=0 mult=1 m=1
XM25 net19 net19 net29 VDD sky130_fd_pr__pfet_01v8 L={L} W={W/2} nf=1 ad='int((nf+1)/2) * W/nf * 0.29'
+ as='int((nf+2)/2) * W/nf * 0.29' pd='2*int((nf+1)/2) * (W/nf + 0.29)' ps='2*int((nf+2)/2) * (W/nf + 0.29)'
+ nrd='0.29 / W' nrs='0.29 / W' sa=0 sb=0 sd=0 mult=1 m=1
XM26 net29 net19 net28 VDD sky130_fd_pr__pfet_01v8 L={L} W={W/2} nf=1 ad='int((nf+1)/2) * W/nf * 0.29'
+ as='int((nf+2)/2) * W/nf * 0.29' pd='2*int((nf+1)/2) * (W/nf + 0.29)' ps='2*int((nf+2)/2) * (W/nf + 0.29)'
+ nrd='0.29 / W' nrs='0.29 / W' sa=0 sb=0 sd=0 mult=1 m=1
XM27 net28 net19 net27 VDD sky130_fd_pr__pfet_01v8 L={L} W={W/2} nf=1 ad='int((nf+1)/2) * W/nf * 0.29'
+ as='int((nf+2)/2) * W/nf * 0.29' pd='2*int((nf+1)/2) * (W/nf + 0.29)' ps='2*int((nf+2)/2) * (W/nf + 0.29)'
+ nrd='0.29 / W' nrs='0.29 / W' sa=0 sb=0 sd=0 mult=1 m=1
XM28 net27 net19 net25 VDD sky130_fd_pr__pfet_01v8 L={L} W={W/2} nf=1 ad='int((nf+1)/2) * W/nf * 0.29'
+ as='int((nf+2)/2) * W/nf * 0.29' pd='2*int((nf+1)/2) * (W/nf + 0.29)' ps='2*int((nf+2)/2) * (W/nf + 0.29)'
+ nrd='0.29 / W' nrs='0.29 / W' sa=0 sb=0 sd=0 mult=1 m=1
XM30 net23 net22 net38 VDD sky130_fd_pr__pfet_01v8 L={L} W={W/2} nf=1 ad='int((nf+1)/2) * W/nf * 0.29'
+ as='int((nf+2)/2) * W/nf * 0.29' pd='2*int((nf+1)/2) * (W/nf + 0.29)' ps='2*int((nf+2)/2) * (W/nf + 0.29)'
+ nrd='0.29 / W' nrs='0.29 / W' sa=0 sb=0 sd=0 mult=1 m=1
XM31 net38 net22 net37 VDD sky130_fd_pr__pfet_01v8 L={L} W={W/2} nf=1 ad='int((nf+1)/2) * W/nf * 0.29'
+ as='int((nf+2)/2) * W/nf * 0.29' pd='2*int((nf+1)/2) * (W/nf + 0.29)' ps='2*int((nf+2)/2) * (W/nf + 0.29)'
+ nrd='0.29 / W' nrs='0.29 / W' sa=0 sb=0 sd=0 mult=1 m=1
XM32 net37 net22 net36 VDD sky130_fd_pr__pfet_01v8 L={L} W={W/2} nf=1 ad='int((nf+1)/2) * W/nf * 0.29'
+ as='int((nf+2)/2) * W/nf * 0.29' pd='2*int((nf+1)/2) * (W/nf + 0.29)' ps='2*int((nf+2)/2) * (W/nf + 0.29)'
+ nrd='0.29 / W' nrs='0.29 / W' sa=0 sb=0 sd=0 mult=1 m=1
XM33 net36 net22 net22 VDD sky130_fd_pr__pfet_01v8 L={L} W={W/2} nf=1 ad='int((nf+1)/2) * W/nf * 0.29'
+ as='int((nf+2)/2) * W/nf * 0.29' pd='2*int((nf+1)/2) * (W/nf + 0.29)' ps='2*int((nf+2)/2) * (W/nf + 0.29)'
+ nrd='0.29 / W' nrs='0.29 / W' sa=0 sb=0 sd=0 mult=1 m=1
XM34 net22 net22 net35 VDD sky130_fd_pr__pfet_01v8 L={L} W={W/2} nf=1 ad='int((nf+1)/2) * W/nf * 0.29'
+ as='int((nf+2)/2) * W/nf * 0.29' pd='2*int((nf+1)/2) * (W/nf + 0.29)' ps='2*int((nf+2)/2) * (W/nf + 0.29)'
+ nrd='0.29 / W' nrs='0.29 / W' sa=0 sb=0 sd=0 mult=1 m=1
XM35 net35 net22 net34 VDD sky130_fd_pr__pfet_01v8 L={L} W={W/2} nf=1 ad='int((nf+1)/2) * W/nf * 0.29'
+ as='int((nf+2)/2) * W/nf * 0.29' pd='2*int((nf+1)/2) * (W/nf + 0.29)' ps='2*int((nf+2)/2) * (W/nf + 0.29)'
+ nrd='0.29 / W' nrs='0.29 / W' sa=0 sb=0 sd=0 mult=1 m=1
XM36 net34 net22 net33 VDD sky130_fd_pr__pfet_01v8 L={L} W={W/2} nf=1 ad='int((nf+1)/2) * W/nf * 0.29'
+ as='int((nf+2)/2) * W/nf * 0.29' pd='2*int((nf+1)/2) * (W/nf + 0.29)' ps='2*int((nf+2)/2) * (W/nf + 0.29)'
+ nrd='0.29 / W' nrs='0.29 / W' sa=0 sb=0 sd=0 mult=1 m=1
XM37 net33 net22 net23 VDD sky130_fd_pr__pfet_01v8 L={L} W={W/2} nf=1 ad='int((nf+1)/2) * W/nf * 0.29'
+ as='int((nf+2)/2) * W/nf * 0.29' pd='2*int((nf+1)/2) * (W/nf + 0.29)' ps='2*int((nf+2)/2) * (W/nf + 0.29)'
+ nrd='0.29 / W' nrs='0.29 / W' sa=0 sb=0 sd=0 mult=1 m=1
XM38 VDD net41 net2 VDD sky130_fd_pr__pfet_01v8 L={L} W={W/2} nf=1 ad='int((nf+1)/2) * W/nf * 0.29' as='int((nf+2)/2) * W/nf * 0.29'
+ pd='2*int((nf+1)/2) * (W/nf + 0.29)' ps='2*int((nf+2)/2) * (W/nf + 0.29)' nrd='0.29 / W' nrs='0.29 / W'
+ sa=0 sb=0 sd=0 mult=1 m=1
XM39 VDD VDD net2 VDD sky130_fd_pr__pfet_01v8 L={L} W={W/2} nf=1 ad='int((nf+1)/2) * W/nf * 0.29' as='int((nf+2)/2) * W/nf * 0.29'
+ pd='2*int((nf+1)/2) * (W/nf + 0.29)' ps='2*int((nf+2)/2) * (W/nf + 0.29)' nrd='0.29 / W' nrs='0.29 / W'
+ sa=0 sb=0 sd=0 mult=1 m=1
XM96 net41 net41 VDD VDD sky130_fd_pr__pfet_01v8 L={L} W={W/2} nf=1 ad='int((nf+1)/2) * W/nf * 0.29'
+ as='int((nf+2)/2) * W/nf * 0.29' pd='2*int((nf+1)/2) * (W/nf + 0.29)' ps='2*int((nf+2)/2) * (W/nf + 0.29)'
+ nrd='0.29 / W' nrs='0.29 / W' sa=0 sb=0 sd=0 mult=1 m=1
XM97 VDD net41 net48 VDD sky130_fd_pr__pfet_01v8 L={L} W={W/2} nf=1 ad='int((nf+1)/2) * W/nf * 0.29'
+ as='int((nf+2)/2) * W/nf * 0.29' pd='2*int((nf+1)/2) * (W/nf + 0.29)' ps='2*int((nf+2)/2) * (W/nf + 0.29)'
+ nrd='0.29 / W' nrs='0.29 / W' sa=0 sb=0 sd=0 mult=1 m=1
XM98 net44 net41 VDD VDD sky130_fd_pr__pfet_01v8 L={L} W={W/2} nf=1 ad='int((nf+1)/2) * W/nf * 0.29'
+ as='int((nf+2)/2) * W/nf * 0.29' pd='2*int((nf+1)/2) * (W/nf + 0.29)' ps='2*int((nf+2)/2) * (W/nf + 0.29)'
+ nrd='0.29 / W' nrs='0.29 / W' sa=0 sb=0 sd=0 mult=1 m=1
XM99 VDD net41 net41 VDD sky130_fd_pr__pfet_01v8 L={L} W={W/2} nf=1 ad='int((nf+1)/2) * W/nf * 0.29'
+ as='int((nf+2)/2) * W/nf * 0.29' pd='2*int((nf+1)/2) * (W/nf + 0.29)' ps='2*int((nf+2)/2) * (W/nf + 0.29)'
+ nrd='0.29 / W' nrs='0.29 / W' sa=0 sb=0 sd=0 mult=1 m=1
XM100 net2 net41 VDD VDD sky130_fd_pr__pfet_01v8 L={L} W={W/2} nf=1 ad='int((nf+1)/2) * W/nf * 0.29'
+ as='int((nf+2)/2) * W/nf * 0.29' pd='2*int((nf+1)/2) * (W/nf + 0.29)' ps='2*int((nf+2)/2) * (W/nf + 0.29)'
+ nrd='0.29 / W' nrs='0.29 / W' sa=0 sb=0 sd=0 mult=1 m=1
XM101 net2 VDD VDD VDD sky130_fd_pr__pfet_01v8 L={L} W={W/2} nf=1 ad='int((nf+1)/2) * W/nf * 0.29' as='int((nf+2)/2) * W/nf * 0.29'
+ pd='2*int((nf+1)/2) * (W/nf + 0.29)' ps='2*int((nf+2)/2) * (W/nf + 0.29)' nrd='0.29 / W' nrs='0.29 / W'
+ sa=0 sb=0 sd=0 mult=1 m=1
XM110 net43 net42 GND GND sky130_fd_pr__nfet_01v8 L={L} W={W/2} nf=1 ad='int((nf+1)/2) * W/nf * 0.29'
+ as='int((nf+2)/2) * W/nf * 0.29' pd='2*int((nf+1)/2) * (W/nf + 0.29)' ps='2*int((nf+2)/2) * (W/nf + 0.29)'
+ nrd='0.29 / W' nrs='0.29 / W' sa=0 sb=0 sd=0 mult=1 m=1
XM112 GND GND net41 GND sky130_fd_pr__nfet_01v8 L={L} W={W/2} nf=1 ad='int((nf+1)/2) * W/nf * 0.29' as='int((nf+2)/2) * W/nf * 0.29'
+ pd='2*int((nf+1)/2) * (W/nf + 0.29)' ps='2*int((nf+2)/2) * (W/nf + 0.29)' nrd='0.29 / W' nrs='0.29 / W'
+ sa=0 sb=0 sd=0 mult=1 m=1
XM113 GND GND GND GND sky130_fd_pr__nfet_01v8 L={L} W={W/2} nf=1 ad='int((nf+1)/2) * W/nf * 0.29' as='int((nf+2)/2) * W/nf * 0.29'
+ pd='2*int((nf+1)/2) * (W/nf + 0.29)' ps='2*int((nf+2)/2) * (W/nf + 0.29)' nrd='0.29 / W' nrs='0.29 / W'
+ sa=0 sb=0 sd=0 mult=1 m=1
XM120 net41 GND GND GND sky130_fd_pr__nfet_01v8 L={L} W={W/2} nf=1 ad='int((nf+1)/2) * W/nf * 0.29' as='int((nf+2)/2) * W/nf * 0.29'
+ pd='2*int((nf+1)/2) * (W/nf + 0.29)' ps='2*int((nf+2)/2) * (W/nf + 0.29)' nrd='0.29 / W' nrs='0.29 / W'
+ sa=0 sb=0 sd=0 mult=1 m=1
XM121 GND GND GND GND sky130_fd_pr__nfet_01v8 L={L} W={W/2} nf=1 ad='int((nf+1)/2) * W/nf * 0.29' as='int((nf+2)/2) * W/nf * 0.29'
+ pd='2*int((nf+1)/2) * (W/nf + 0.29)' ps='2*int((nf+2)/2) * (W/nf + 0.29)' nrd='0.29 / W' nrs='0.29 / W'
+ sa=0 sb=0 sd=0 mult=1 m=1
XM40 net42 net42 net43 GND sky130_fd_pr__nfet_01v8 L={L} W={W/2} nf=1 ad='int((nf+1)/2) * W/nf * 0.29'
+ as='int((nf+2)/2) * W/nf * 0.29' pd='2*int((nf+1)/2) * (W/nf + 0.29)' ps='2*int((nf+2)/2) * (W/nf + 0.29)'
+ nrd='0.29 / W' nrs='0.29 / W' sa=0 sb=0 sd=0 mult=1 m=1
XM41 net43 net42 net42 GND sky130_fd_pr__nfet_01v8 L={L} W={W/2} nf=1 ad='int((nf+1)/2) * W/nf * 0.29'
+ as='int((nf+2)/2) * W/nf * 0.29' pd='2*int((nf+1)/2) * (W/nf + 0.29)' ps='2*int((nf+2)/2) * (W/nf + 0.29)'
+ nrd='0.29 / W' nrs='0.29 / W' sa=0 sb=0 sd=0 mult=1 m=1
XM42 net42 net42 net43 GND sky130_fd_pr__nfet_01v8 L={L} W={W/2} nf=1 ad='int((nf+1)/2) * W/nf * 0.29'
+ as='int((nf+2)/2) * W/nf * 0.29' pd='2*int((nf+1)/2) * (W/nf + 0.29)' ps='2*int((nf+2)/2) * (W/nf + 0.29)'
+ nrd='0.29 / W' nrs='0.29 / W' sa=0 sb=0 sd=0 mult=1 m=1
XM43 net43 net42 net42 GND sky130_fd_pr__nfet_01v8 L={L} W={W/2} nf=1 ad='int((nf+1)/2) * W/nf * 0.29'
+ as='int((nf+2)/2) * W/nf * 0.29' pd='2*int((nf+1)/2) * (W/nf + 0.29)' ps='2*int((nf+2)/2) * (W/nf + 0.29)'
+ nrd='0.29 / W' nrs='0.29 / W' sa=0 sb=0 sd=0 mult=1 m=1
XM44 net42 net42 net43 GND sky130_fd_pr__nfet_01v8 L={L} W={W/2} nf=1 ad='int((nf+1)/2) * W/nf * 0.29'
+ as='int((nf+2)/2) * W/nf * 0.29' pd='2*int((nf+1)/2) * (W/nf + 0.29)' ps='2*int((nf+2)/2) * (W/nf + 0.29)'
+ nrd='0.29 / W' nrs='0.29 / W' sa=0 sb=0 sd=0 mult=1 m=1
XM45 net43 net42 net42 GND sky130_fd_pr__nfet_01v8 L={L} W={W/2} nf=1 ad='int((nf+1)/2) * W/nf * 0.29'
+ as='int((nf+2)/2) * W/nf * 0.29' pd='2*int((nf+1)/2) * (W/nf + 0.29)' ps='2*int((nf+2)/2) * (W/nf + 0.29)'
+ nrd='0.29 / W' nrs='0.29 / W' sa=0 sb=0 sd=0 mult=1 m=1
XM46 net42 net42 net43 GND sky130_fd_pr__nfet_01v8 L={L} W={W/2} nf=1 ad='int((nf+1)/2) * W/nf * 0.29'
+ as='int((nf+2)/2) * W/nf * 0.29' pd='2*int((nf+1)/2) * (W/nf + 0.29)' ps='2*int((nf+2)/2) * (W/nf + 0.29)'
+ nrd='0.29 / W' nrs='0.29 / W' sa=0 sb=0 sd=0 mult=1 m=1
XM102 net43 net42 net42 GND sky130_fd_pr__nfet_01v8 L={L} W={W/2} nf=1 ad='int((nf+1)/2) * W/nf * 0.29'
+ as='int((nf+2)/2) * W/nf * 0.29' pd='2*int((nf+1)/2) * (W/nf + 0.29)' ps='2*int((nf+2)/2) * (W/nf + 0.29)'
+ nrd='0.29 / W' nrs='0.29 / W' sa=0 sb=0 sd=0 mult=1 m=1
XM103 GND net42 net43 GND sky130_fd_pr__nfet_01v8 L={L} W={W/2} nf=1 ad='int((nf+1)/2) * W/nf * 0.29'
+ as='int((nf+2)/2) * W/nf * 0.29' pd='2*int((nf+1)/2) * (W/nf + 0.29)' ps='2*int((nf+2)/2) * (W/nf + 0.29)'
+ nrd='0.29 / W' nrs='0.29 / W' sa=0 sb=0 sd=0 mult=1 m=1
XM104 GND Vbn net41 GND sky130_fd_pr__nfet_01v8 L={L} W={W/2} nf=1 ad='int((nf+1)/2) * W/nf * 0.29' as='int((nf+2)/2) * W/nf * 0.29'
+ pd='2*int((nf+1)/2) * (W/nf + 0.29)' ps='2*int((nf+2)/2) * (W/nf + 0.29)' nrd='0.29 / W' nrs='0.29 / W'
+ sa=0 sb=0 sd=0 mult=1 m=1
XM105 net41 Vbn GND GND sky130_fd_pr__nfet_01v8 L={L} W={W/2} nf=1 ad='int((nf+1)/2) * W/nf * 0.29' as='int((nf+2)/2) * W/nf * 0.29'
+ pd='2*int((nf+1)/2) * (W/nf + 0.29)' ps='2*int((nf+2)/2) * (W/nf + 0.29)' nrd='0.29 / W' nrs='0.29 / W'
+ sa=0 sb=0 sd=0 mult=1 m=1
XM106 net48 net41 net49 VDD sky130_fd_pr__pfet_01v8 L={L} W={W/2} nf=1 ad='int((nf+1)/2) * W/nf * 0.29'
+ as='int((nf+2)/2) * W/nf * 0.29' pd='2*int((nf+1)/2) * (W/nf + 0.29)' ps='2*int((nf+2)/2) * (W/nf + 0.29)'
+ nrd='0.29 / W' nrs='0.29 / W' sa=0 sb=0 sd=0 mult=1 m=1
XM107 net49 net41 net50 VDD sky130_fd_pr__pfet_01v8 L={L} W={W/2} nf=1 ad='int((nf+1)/2) * W/nf * 0.29'
+ as='int((nf+2)/2) * W/nf * 0.29' pd='2*int((nf+1)/2) * (W/nf + 0.29)' ps='2*int((nf+2)/2) * (W/nf + 0.29)'
+ nrd='0.29 / W' nrs='0.29 / W' sa=0 sb=0 sd=0 mult=1 m=1
XM108 net50 net41 net51 VDD sky130_fd_pr__pfet_01v8 L={L} W={W/2} nf=1 ad='int((nf+1)/2) * W/nf * 0.29'
+ as='int((nf+2)/2) * W/nf * 0.29' pd='2*int((nf+1)/2) * (W/nf + 0.29)' ps='2*int((nf+2)/2) * (W/nf + 0.29)'
+ nrd='0.29 / W' nrs='0.29 / W' sa=0 sb=0 sd=0 mult=1 m=1
XM109 net51 net41 net42 VDD sky130_fd_pr__pfet_01v8 L={L} W={W/2} nf=1 ad='int((nf+1)/2) * W/nf * 0.29'
+ as='int((nf+2)/2) * W/nf * 0.29' pd='2*int((nf+1)/2) * (W/nf + 0.29)' ps='2*int((nf+2)/2) * (W/nf + 0.29)'
+ nrd='0.29 / W' nrs='0.29 / W' sa=0 sb=0 sd=0 mult=1 m=1
XM111 net42 net41 net47 VDD sky130_fd_pr__pfet_01v8 L={L} W={W/2} nf=1 ad='int((nf+1)/2) * W/nf * 0.29'
+ as='int((nf+2)/2) * W/nf * 0.29' pd='2*int((nf+1)/2) * (W/nf + 0.29)' ps='2*int((nf+2)/2) * (W/nf + 0.29)'
+ nrd='0.29 / W' nrs='0.29 / W' sa=0 sb=0 sd=0 mult=1 m=1
XM114 net47 net41 net46 VDD sky130_fd_pr__pfet_01v8 L={L} W={W/2} nf=1 ad='int((nf+1)/2) * W/nf * 0.29'
+ as='int((nf+2)/2) * W/nf * 0.29' pd='2*int((nf+1)/2) * (W/nf + 0.29)' ps='2*int((nf+2)/2) * (W/nf + 0.29)'
+ nrd='0.29 / W' nrs='0.29 / W' sa=0 sb=0 sd=0 mult=1 m=1
XM115 net46 net41 net45 VDD sky130_fd_pr__pfet_01v8 L={L} W={W/2} nf=1 ad='int((nf+1)/2) * W/nf * 0.29'
+ as='int((nf+2)/2) * W/nf * 0.29' pd='2*int((nf+1)/2) * (W/nf + 0.29)' ps='2*int((nf+2)/2) * (W/nf + 0.29)'
+ nrd='0.29 / W' nrs='0.29 / W' sa=0 sb=0 sd=0 mult=1 m=1
XM116 net45 net41 net44 VDD sky130_fd_pr__pfet_01v8 L={L} W={W/2} nf=1 ad='int((nf+1)/2) * W/nf * 0.29'
+ as='int((nf+2)/2) * W/nf * 0.29' pd='2*int((nf+1)/2) * (W/nf + 0.29)' ps='2*int((nf+2)/2) * (W/nf + 0.29)'
+ nrd='0.29 / W' nrs='0.29 / W' sa=0 sb=0 sd=0 mult=1 m=1
XM117 net43 GND GND GND sky130_fd_pr__nfet_01v8 L={L} W={W/2} nf=1 ad='int((nf+1)/2) * W/nf * 0.29' as='int((nf+2)/2) * W/nf * 0.29'
+ pd='2*int((nf+1)/2) * (W/nf + 0.29)' ps='2*int((nf+2)/2) * (W/nf + 0.29)' nrd='0.29 / W' nrs='0.29 / W'
+ sa=0 sb=0 sd=0 mult=1 m=1
XM118 net2 net2 net43 GND sky130_fd_pr__nfet_01v8 L={L} W={W/2} nf=1 ad='int((nf+1)/2) * W/nf * 0.29'
+ as='int((nf+2)/2) * W/nf * 0.29' pd='2*int((nf+1)/2) * (W/nf + 0.29)' ps='2*int((nf+2)/2) * (W/nf + 0.29)'
+ nrd='0.29 / W' nrs='0.29 / W' sa=0 sb=0 sd=0 mult=1 m=1
XM119 net43 net2 net2 GND sky130_fd_pr__nfet_01v8 L={L} W={W/2} nf=1 ad='int((nf+1)/2) * W/nf * 0.29'
+ as='int((nf+2)/2) * W/nf * 0.29' pd='2*int((nf+1)/2) * (W/nf + 0.29)' ps='2*int((nf+2)/2) * (W/nf + 0.29)'
+ nrd='0.29 / W' nrs='0.29 / W' sa=0 sb=0 sd=0 mult=1 m=1
XM122 GND GND net43 GND sky130_fd_pr__nfet_01v8 L={L} W={W/2} nf=1 ad='int((nf+1)/2) * W/nf * 0.29' as='int((nf+2)/2) * W/nf * 0.29'
+ pd='2*int((nf+1)/2) * (W/nf + 0.29)' ps='2*int((nf+2)/2) * (W/nf + 0.29)' nrd='0.29 / W' nrs='0.29 / W'
+ sa=0 sb=0 sd=0 mult=1 m=1
**** begin user architecture code

.param W=24
.param L=1
.control
set wr_vecnames
set wr_singlescale
let code = 0
  while code < 128
    if code eq 0
      let b0 = 0
    else
      let b0 = code % 2 * 1.8
    end
    if floor(code / 2) eq 0
      let b1 = 0
    else
      let b1 = floor(code / 2) % 2 * 1.8
    end
    if floor(code / 4) eq 0
      let b2 = 0
    else
      let b2 = floor(code / 4) % 2 * 1.8
    end
    if floor(code / 8) eq 0
      let b3 = 0
    else
      let b3 = floor(code / 8) % 2 * 1.8
    end
    if floor(code / 16) eq 0
      let b4 = 0
    else
      let b4 = floor(code / 16) % 2 * 1.8
    end
    if floor(code / 32) eq 0
      let b5 = 0
    else
      let b5 = floor(code / 32) % 2 * 1.8
    end
    if floor(code / 64) eq 0
      let b6 = 0
    else
      let b6 = floor(code / 64) % 2 * 1.8
    end
    alter v0 $&b0
    alter v1 $&b1
    alter v2 $&b2
    alter v3 $&b3
    alter v4 $&b4
    alter v5 $&b5
    alter v6 $&b6
    save all
    op
    wrdata ~/Documents/current-output-dac-vlsi/simulations/dac_sim.txt v(Vbn) i(Vout) i(Vout1) v(b6)
+ v(b5) v(b4) v(b3) v(b2) v(b1) v(b0) v(b0out) v(b1out) v(b6out)
    if code eq 0
      set appendwrite
      set wr_vecnames = FALSE
    end
    let code = code + 1
  end
.endc


.option wnflag=1
.param MC_SWITCH=0.0
.lib ~/skywater/skywater-pdk/libraries/sky130_fd_pr_ngspice/latest/models/sky130.lib.spice tt

**** end user architecture code
**.ends

* expanding   symbol:  /home/madvlsi/Documents/current-output-dac-vlsi/schematics/mux.sym # of
*+ pins=4
** sym_path: /home/madvlsi/Documents/current-output-dac-vlsi/schematics/mux.sym
** sch_path: /home/madvlsi/Documents/current-output-dac-vlsi/schematics/mux.sch
.subckt mux A B Y S
*.ipin S
*.ipin A
*.opin Y
*.ipin B
XM1 net1 S GND GND sky130_fd_pr__nfet_01v8 L=0.15 W=1 nf=1 ad='int((nf+1)/2) * W/nf * 0.29' as='int((nf+2)/2) * W/nf * 0.29'
+ pd='2*int((nf+1)/2) * (W/nf + 0.29)' ps='2*int((nf+2)/2) * (W/nf + 0.29)' nrd='0.29 / W' nrs='0.29 / W'
+ sa=0 sb=0 sd=0 mult=1 m=1
XM2 net1 S VDD VDD sky130_fd_pr__pfet_01v8 L=0.15 W=1 nf=1 ad='int((nf+1)/2) * W/nf * 0.29' as='int((nf+2)/2) * W/nf * 0.29'
+ pd='2*int((nf+1)/2) * (W/nf + 0.29)' ps='2*int((nf+2)/2) * (W/nf + 0.29)' nrd='0.29 / W' nrs='0.29 / W'
+ sa=0 sb=0 sd=0 mult=1 m=1
XM3 Y S B GND sky130_fd_pr__nfet_01v8 L=0.15 W=1 nf=1 ad='int((nf+1)/2) * W/nf * 0.29' as='int((nf+2)/2) * W/nf * 0.29'
+ pd='2*int((nf+1)/2) * (W/nf + 0.29)' ps='2*int((nf+2)/2) * (W/nf + 0.29)' nrd='0.29 / W' nrs='0.29 / W'
+ sa=0 sb=0 sd=0 mult=1 m=1
XM4 A net1 Y GND sky130_fd_pr__nfet_01v8 L=0.15 W=1 nf=1 ad='int((nf+1)/2) * W/nf * 0.29' as='int((nf+2)/2) * W/nf * 0.29'
+ pd='2*int((nf+1)/2) * (W/nf + 0.29)' ps='2*int((nf+2)/2) * (W/nf + 0.29)' nrd='0.29 / W' nrs='0.29 / W'
+ sa=0 sb=0 sd=0 mult=1 m=1
.ends

.GLOBAL GND
.GLOBAL VDD
.end
